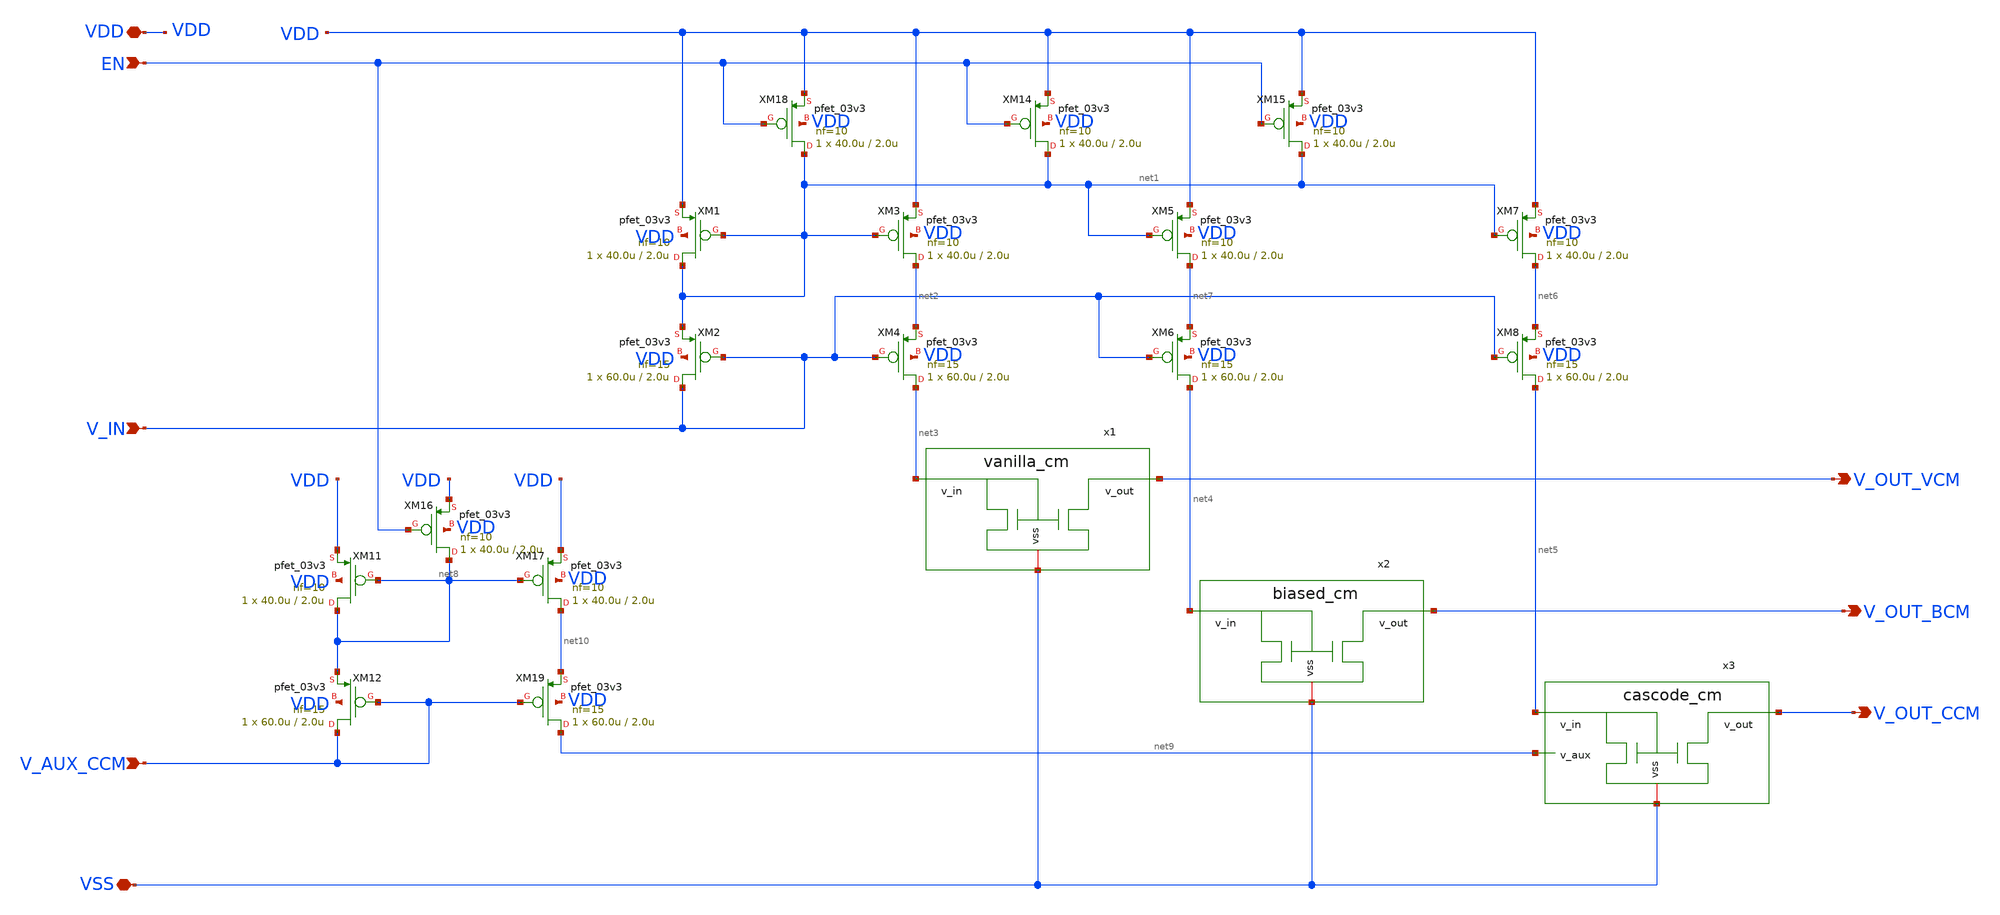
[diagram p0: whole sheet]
** sch_path: blocks/composite/regulated_cascoded_cmirror/xschem/top_level.sch
**.subckt top_level VSS V_AUX_CCM VDD V_OUT_VCM V_OUT_BCM V_OUT_CCM V_IN EN
*.iopin VSS
*.ipin V_AUX_CCM
*.iopin VDD
*.opin V_OUT_VCM
*.opin V_OUT_BCM
*.opin V_OUT_CCM
*.ipin V_IN
*.ipin EN
XM1 net1 net1 VDD VDD pfet_03v3 L=2.0u W=40.0u nf=10 ad='int((nf+1)/2) * W/nf * 0.18u' as='int((nf+2)/2) * W/nf * 0.18u'
+ pd='2*int((nf+1)/2) * (W/nf + 0.18u)' ps='2*int((nf+2)/2) * (W/nf + 0.18u)' nrd='0.18u / W' nrs='0.18u / W'
+ sa=0 sb=0 sd=0 m=1
XM2 V_IN V_IN net1 VDD pfet_03v3 L=2.0u W=60.0u nf=15 ad='int((nf+1)/2) * W/nf * 0.18u' as='int((nf+2)/2) * W/nf * 0.18u'
+ pd='2*int((nf+1)/2) * (W/nf + 0.18u)' ps='2*int((nf+2)/2) * (W/nf + 0.18u)' nrd='0.18u / W' nrs='0.18u / W'
+ sa=0 sb=0 sd=0 m=1
XM3 net2 net1 VDD VDD pfet_03v3 L=2.0u W=40.0u nf=10 ad='int((nf+1)/2) * W/nf * 0.18u' as='int((nf+2)/2) * W/nf * 0.18u'
+ pd='2*int((nf+1)/2) * (W/nf + 0.18u)' ps='2*int((nf+2)/2) * (W/nf + 0.18u)' nrd='0.18u / W' nrs='0.18u / W'
+ sa=0 sb=0 sd=0 m=1
XM4 net3 V_IN net2 VDD pfet_03v3 L=2.0u W=60.0u nf=15 ad='int((nf+1)/2) * W/nf * 0.18u' as='int((nf+2)/2) * W/nf * 0.18u'
+ pd='2*int((nf+1)/2) * (W/nf + 0.18u)' ps='2*int((nf+2)/2) * (W/nf + 0.18u)' nrd='0.18u / W' nrs='0.18u / W'
+ sa=0 sb=0 sd=0 m=1
XM5 net7 net1 VDD VDD pfet_03v3 L=2.0u W=40.0u nf=10 ad='int((nf+1)/2) * W/nf * 0.18u' as='int((nf+2)/2) * W/nf * 0.18u'
+ pd='2*int((nf+1)/2) * (W/nf + 0.18u)' ps='2*int((nf+2)/2) * (W/nf + 0.18u)' nrd='0.18u / W' nrs='0.18u / W'
+ sa=0 sb=0 sd=0 m=1
XM6 net4 V_IN net7 VDD pfet_03v3 L=2.0u W=60.0u nf=15 ad='int((nf+1)/2) * W/nf * 0.18u' as='int((nf+2)/2) * W/nf * 0.18u'
+ pd='2*int((nf+1)/2) * (W/nf + 0.18u)' ps='2*int((nf+2)/2) * (W/nf + 0.18u)' nrd='0.18u / W' nrs='0.18u / W'
+ sa=0 sb=0 sd=0 m=1
XM7 net6 net1 VDD VDD pfet_03v3 L=2.0u W=40.0u nf=10 ad='int((nf+1)/2) * W/nf * 0.18u' as='int((nf+2)/2) * W/nf * 0.18u'
+ pd='2*int((nf+1)/2) * (W/nf + 0.18u)' ps='2*int((nf+2)/2) * (W/nf + 0.18u)' nrd='0.18u / W' nrs='0.18u / W'
+ sa=0 sb=0 sd=0 m=1
XM8 net5 V_IN net6 VDD pfet_03v3 L=2.0u W=60.0u nf=15 ad='int((nf+1)/2) * W/nf * 0.18u' as='int((nf+2)/2) * W/nf * 0.18u'
+ pd='2*int((nf+1)/2) * (W/nf + 0.18u)' ps='2*int((nf+2)/2) * (W/nf + 0.18u)' nrd='0.18u / W' nrs='0.18u / W'
+ sa=0 sb=0 sd=0 m=1
XM11 net8 net8 VDD VDD pfet_03v3 L=2.0u W=40.0u nf=10 ad='int((nf+1)/2) * W/nf * 0.18u' as='int((nf+2)/2) * W/nf * 0.18u'
+ pd='2*int((nf+1)/2) * (W/nf + 0.18u)' ps='2*int((nf+2)/2) * (W/nf + 0.18u)' nrd='0.18u / W' nrs='0.18u / W'
+ sa=0 sb=0 sd=0 m=1
XM12 V_AUX_CCM V_AUX_CCM net8 VDD pfet_03v3 L=2.0u W=60.0u nf=15 ad='int((nf+1)/2) * W/nf * 0.18u' as='int((nf+2)/2) * W/nf * 0.18u'
+ pd='2*int((nf+1)/2) * (W/nf + 0.18u)' ps='2*int((nf+2)/2) * (W/nf + 0.18u)' nrd='0.18u / W' nrs='0.18u / W'
+ sa=0 sb=0 sd=0 m=1
XM14 net1 EN VDD VDD pfet_03v3 L=2.0u W=40.0u nf=10 ad='int((nf+1)/2) * W/nf * 0.18u' as='int((nf+2)/2) * W/nf * 0.18u'
+ pd='2*int((nf+1)/2) * (W/nf + 0.18u)' ps='2*int((nf+2)/2) * (W/nf + 0.18u)' nrd='0.18u / W' nrs='0.18u / W'
+ sa=0 sb=0 sd=0 m=1
XM18 net1 EN VDD VDD pfet_03v3 L=2.0u W=40.0u nf=10 ad='int((nf+1)/2) * W/nf * 0.18u' as='int((nf+2)/2) * W/nf * 0.18u'
+ pd='2*int((nf+1)/2) * (W/nf + 0.18u)' ps='2*int((nf+2)/2) * (W/nf + 0.18u)' nrd='0.18u / W' nrs='0.18u / W'
+ sa=0 sb=0 sd=0 m=1
XM15 net1 EN VDD VDD pfet_03v3 L=2.0u W=40.0u nf=10 ad='int((nf+1)/2) * W/nf * 0.18u' as='int((nf+2)/2) * W/nf * 0.18u'
+ pd='2*int((nf+1)/2) * (W/nf + 0.18u)' ps='2*int((nf+2)/2) * (W/nf + 0.18u)' nrd='0.18u / W' nrs='0.18u / W'
+ sa=0 sb=0 sd=0 m=1
XM16 net8 EN VDD VDD pfet_03v3 L=2.0u W=40.0u nf=10 ad='int((nf+1)/2) * W/nf * 0.18u' as='int((nf+2)/2) * W/nf * 0.18u'
+ pd='2*int((nf+1)/2) * (W/nf + 0.18u)' ps='2*int((nf+2)/2) * (W/nf + 0.18u)' nrd='0.18u / W' nrs='0.18u / W'
+ sa=0 sb=0 sd=0 m=1
XM17 net10 net8 VDD VDD pfet_03v3 L=2.0u W=40.0u nf=10 ad='int((nf+1)/2) * W/nf * 0.18u' as='int((nf+2)/2) * W/nf * 0.18u'
+ pd='2*int((nf+1)/2) * (W/nf + 0.18u)' ps='2*int((nf+2)/2) * (W/nf + 0.18u)' nrd='0.18u / W' nrs='0.18u / W'
+ sa=0 sb=0 sd=0 m=1
XM19 net9 V_AUX_CCM net10 VDD pfet_03v3 L=2.0u W=60.0u nf=15 ad='int((nf+1)/2) * W/nf * 0.18u' as='int((nf+2)/2) * W/nf * 0.18u'
+ pd='2*int((nf+1)/2) * (W/nf + 0.18u)' ps='2*int((nf+2)/2) * (W/nf + 0.18u)' nrd='0.18u / W' nrs='0.18u / W'
+ sa=0 sb=0 sd=0 m=1
x1 net3 V_OUT_VCM VSS vanilla_cm
x2 V_OUT_BCM net4 VSS biased_cm
x3 V_OUT_CCM net9 net5 VSS cascode_cm
**.ends

* expanding   symbol:  vanilla_cm.sym # of pins=3
** sym_path: vanilla_cm.sym
** sch_path: vanilla_cm.sch
.subckt vanilla_cm v_in v_out vss
*.ipin v_in
*.iopin vss
*.opin v_out
XM1 v_out v_in vss vss nfet_03v3 L=1u W=5u nf=1 ad='int((nf+1)/2) * W/nf * 0.18u' as='int((nf+2)/2) * W/nf * 0.18u'
+ pd='2*int((nf+1)/2) * (W/nf + 0.18u)' ps='2*int((nf+2)/2) * (W/nf + 0.18u)' nrd='0.18u / W' nrs='0.18u / W'
+ sa=0 sb=0 sd=0 m=1
XM2 v_in v_in vss vss nfet_03v3 L=1u W=5u nf=1 ad='int((nf+1)/2) * W/nf * 0.18u' as='int((nf+2)/2) * W/nf * 0.18u'
+ pd='2*int((nf+1)/2) * (W/nf + 0.18u)' ps='2*int((nf+2)/2) * (W/nf + 0.18u)' nrd='0.18u / W' nrs='0.18u / W'
+ sa=0 sb=0 sd=0 m=1
.ends


* expanding   symbol:  biased_cm.sym # of pins=3
** sym_path: biased_cm.sym
** sch_path: biased_cm.sch
.subckt biased_cm v_out v_in vss
*.ipin v_in
*.iopin vss
*.opin v_out
XM3 net2 net1 vss vss nfet_03v3 L=1u W=5u nf=1 ad='int((nf+1)/2) * W/nf * 0.18u' as='int((nf+2)/2) * W/nf * 0.18u'
+ pd='2*int((nf+1)/2) * (W/nf + 0.18u)' ps='2*int((nf+2)/2) * (W/nf + 0.18u)' nrd='0.18u / W' nrs='0.18u / W'
+ sa=0 sb=0 sd=0 m=1
XM4 net1 net1 vss vss nfet_03v3 L=1u W=5u nf=1 ad='int((nf+1)/2) * W/nf * 0.18u' as='int((nf+2)/2) * W/nf * 0.18u'
+ pd='2*int((nf+1)/2) * (W/nf + 0.18u)' ps='2*int((nf+2)/2) * (W/nf + 0.18u)' nrd='0.18u / W' nrs='0.18u / W'
+ sa=0 sb=0 sd=0 m=1
XM5 v_out v_in net2 vss nfet_03v3 L=1u W=5u nf=1 ad='int((nf+1)/2) * W/nf * 0.18u' as='int((nf+2)/2) * W/nf * 0.18u'
+ pd='2*int((nf+1)/2) * (W/nf + 0.18u)' ps='2*int((nf+2)/2) * (W/nf + 0.18u)' nrd='0.18u / W' nrs='0.18u / W'
+ sa=0 sb=0 sd=0 m=1
XM6 v_in v_in net1 vss nfet_03v3 L=1u W=5u nf=1 ad='int((nf+1)/2) * W/nf * 0.18u' as='int((nf+2)/2) * W/nf * 0.18u'
+ pd='2*int((nf+1)/2) * (W/nf + 0.18u)' ps='2*int((nf+2)/2) * (W/nf + 0.18u)' nrd='0.18u / W' nrs='0.18u / W'
+ sa=0 sb=0 sd=0 m=1
.ends


* expanding   symbol:  cascode_cm.sym # of pins=4
** sym_path: cascode_cm.sym
** sch_path: cascode_cm.sch
.subckt cascode_cm v_out v_aux v_in vss
*.ipin v_in
*.iopin vss
*.ipin v_aux
*.opin v_out
XM10 v_aux net1 vss vss nfet_03v3 L=1u W=5u nf=1 ad='int((nf+1)/2) * W/nf * 0.18u' as='int((nf+2)/2) * W/nf * 0.18u'
+ pd='2*int((nf+1)/2) * (W/nf + 0.18u)' ps='2*int((nf+2)/2) * (W/nf + 0.18u)' nrd='0.18u / W' nrs='0.18u / W'
+ sa=0 sb=0 sd=0 m=1
XM8 v_in v_aux net1 vss nfet_03v3 L=1u W=5u nf=1 ad='int((nf+1)/2) * W/nf * 0.18u' as='int((nf+2)/2) * W/nf * 0.18u'
+ pd='2*int((nf+1)/2) * (W/nf + 0.18u)' ps='2*int((nf+2)/2) * (W/nf + 0.18u)' nrd='0.18u / W' nrs='0.18u / W'
+ sa=0 sb=0 sd=0 m=1
XM11 net1 v_in vss vss nfet_03v3 L=1u W=5u nf=1 ad='int((nf+1)/2) * W/nf * 0.18u' as='int((nf+2)/2) * W/nf * 0.18u'
+ pd='2*int((nf+1)/2) * (W/nf + 0.18u)' ps='2*int((nf+2)/2) * (W/nf + 0.18u)' nrd='0.18u / W' nrs='0.18u / W'
+ sa=0 sb=0 sd=0 m=1
XM12 v_aux net2 vss vss nfet_03v3 L=1u W=5u nf=1 ad='int((nf+1)/2) * W/nf * 0.18u' as='int((nf+2)/2) * W/nf * 0.18u'
+ pd='2*int((nf+1)/2) * (W/nf + 0.18u)' ps='2*int((nf+2)/2) * (W/nf + 0.18u)' nrd='0.18u / W' nrs='0.18u / W'
+ sa=0 sb=0 sd=0 m=1
XM13 net2 v_in vss vss nfet_03v3 L=1u W=5u nf=1 ad='int((nf+1)/2) * W/nf * 0.18u' as='int((nf+2)/2) * W/nf * 0.18u'
+ pd='2*int((nf+1)/2) * (W/nf + 0.18u)' ps='2*int((nf+2)/2) * (W/nf + 0.18u)' nrd='0.18u / W' nrs='0.18u / W'
+ sa=0 sb=0 sd=0 m=1
XM14 v_out v_aux net2 vss nfet_03v3 L=1u W=5u nf=1 ad='int((nf+1)/2) * W/nf * 0.18u' as='int((nf+2)/2) * W/nf * 0.18u'
+ pd='2*int((nf+1)/2) * (W/nf + 0.18u)' ps='2*int((nf+2)/2) * (W/nf + 0.18u)' nrd='0.18u / W' nrs='0.18u / W'
+ sa=0 sb=0 sd=0 m=1
.ends

.end
